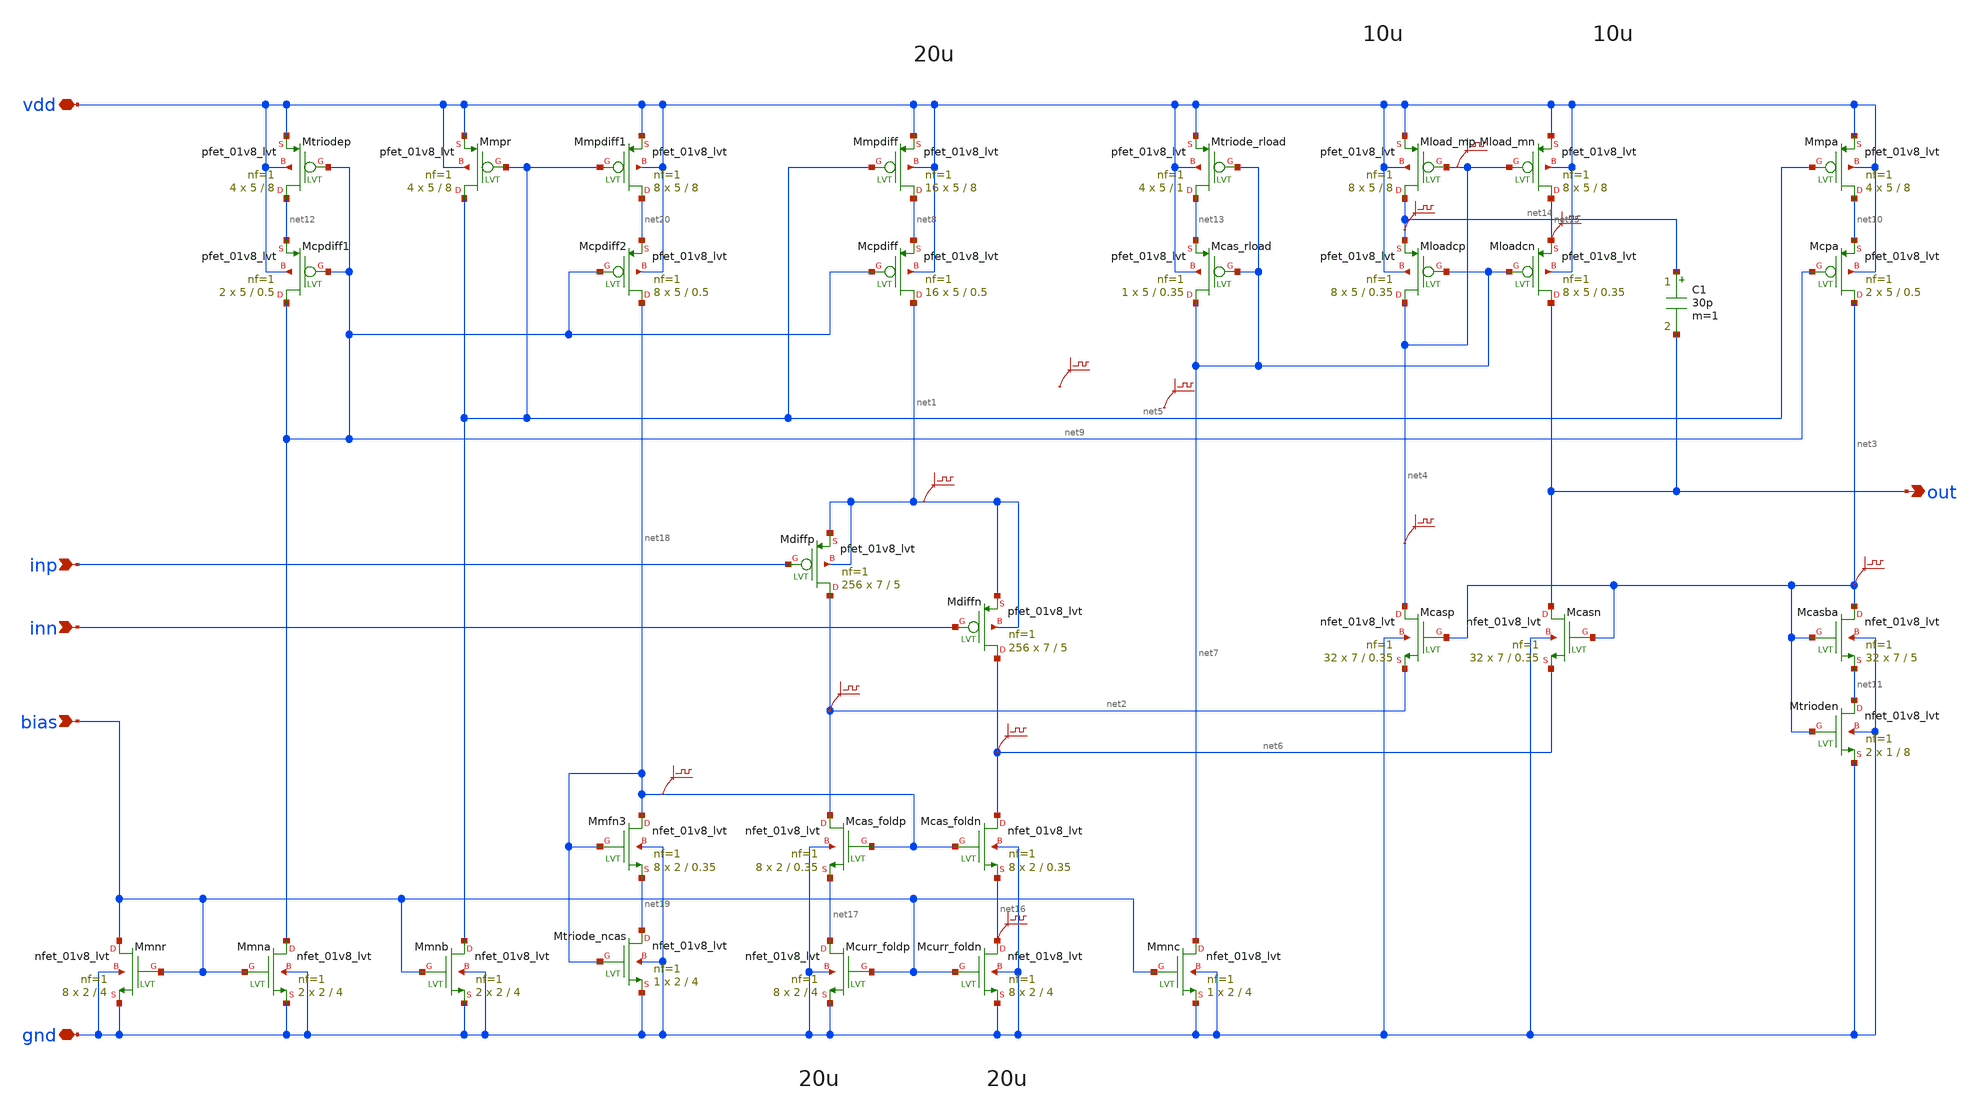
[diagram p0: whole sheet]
** sch_path: design/bandgap_opamp_twostage/bandgap_opamp_twostage.sch
**.subckt bandgap_opamp_twostage inp inn bias out vdd gnd
*.ipin inp
*.ipin inn
*.ipin bias
*.opin out
*.iopin vdd
*.iopin gnd
XMmpdiff net8 net5 vdd vdd sky130_fd_pr__pfet_01v8_lvt L=8 W=5 nf=1 ad='W * 0.29' as='W * 0.29' pd='2 * (W + 0.29)'
+ ps='2 * (W + 0.29)' nrd='0.29 / W' nrs='0.29 / W' sa=0 sb=0 sd=0 mult=16 m=16
XMmpr net5 net5 vdd vdd sky130_fd_pr__pfet_01v8_lvt L=8 W=5 nf=1 ad='W * 0.29' as='W * 0.29' pd='2 * (W + 0.29)'
+ ps='2 * (W + 0.29)' nrd='0.29 / W' nrs='0.29 / W' sa=0 sb=0 sd=0 mult=4 m=4
XMmnr bias bias gnd gnd sky130_fd_pr__nfet_01v8_lvt L=4 W=2 nf=1 ad='W * 0.29' as='W * 0.29' pd='2 * (W + 0.29)'
+ ps='2 * (W + 0.29)' nrd='0.29 / W' nrs='0.29 / W' sa=0 sb=0 sd=0 mult=8 m=8
XMmnb net5 bias gnd gnd sky130_fd_pr__nfet_01v8_lvt L=4 W=2 nf=1 ad='W * 0.29' as='W * 0.29' pd='2 * (W + 0.29)'
+ ps='2 * (W + 0.29)' nrd='0.29 / W' nrs='0.29 / W' sa=0 sb=0 sd=0 mult=2 m=2
XMtrioden net11 net3 gnd gnd sky130_fd_pr__nfet_01v8_lvt L=8 W=1 nf=1 ad='W * 0.29' as='W * 0.29' pd='2 * (W + 0.29)'
+ ps='2 * (W + 0.29)' nrd='0.29 / W' nrs='0.29 / W' sa=0 sb=0 sd=0 mult=2 m=2
XMmpa net10 net5 vdd vdd sky130_fd_pr__pfet_01v8_lvt L=8 W=5 nf=1 ad='W * 0.29' as='W * 0.29' pd='2 * (W + 0.29)'
+ ps='2 * (W + 0.29)' nrd='0.29 / W' nrs='0.29 / W' sa=0 sb=0 sd=0 mult=4 m=4
XMcpdiff net1 net9 net8 vdd sky130_fd_pr__pfet_01v8_lvt L=0.5 W=5 nf=1 ad='W * 0.29' as='W * 0.29' pd='2 * (W + 0.29)'
+ ps='2 * (W + 0.29)' nrd='0.29 / W' nrs='0.29 / W' sa=0 sb=0 sd=0 mult=16 m=16
XMmna net9 bias gnd gnd sky130_fd_pr__nfet_01v8_lvt L=4 W=2 nf=1 ad='W * 0.29' as='W * 0.29' pd='2 * (W + 0.29)'
+ ps='2 * (W + 0.29)' nrd='0.29 / W' nrs='0.29 / W' sa=0 sb=0 sd=0 mult=2 m=2
XMtriodep net12 net9 vdd vdd sky130_fd_pr__pfet_01v8_lvt L=8 W=5 nf=1 ad='W * 0.29' as='W * 0.29' pd='2 * (W + 0.29)'
+ ps='2 * (W + 0.29)' nrd='0.29 / W' nrs='0.29 / W' sa=0 sb=0 sd=0 mult=4 m=4
XMcpa net3 net9 net10 vdd sky130_fd_pr__pfet_01v8_lvt L=0.5 W=5 nf=1 ad='W * 0.29' as='W * 0.29' pd='2 * (W + 0.29)'
+ ps='2 * (W + 0.29)' nrd='0.29 / W' nrs='0.29 / W' sa=0 sb=0 sd=0 mult=2 m=2
XMcasba net3 net3 net11 gnd sky130_fd_pr__nfet_01v8_lvt L=5 W=7 nf=1 ad='W * 0.29' as='W * 0.29' pd='2 * (W + 0.29)'
+ ps='2 * (W + 0.29)' nrd='0.29 / W' nrs='0.29 / W' sa=0 sb=0 sd=0 mult=32 m=32
.save v(net2)
XMcasn out net3 net6 gnd sky130_fd_pr__nfet_01v8_lvt L=0.35 W=7 nf=1 ad='W * 0.29' as='W * 0.29' pd='2 * (W + 0.29)'
+ ps='2 * (W + 0.29)' nrd='0.29 / W' nrs='0.29 / W' sa=0 sb=0 sd=0 mult=32 m=32
XMcasp net4 net3 net2 gnd sky130_fd_pr__nfet_01v8_lvt L=0.35 W=7 nf=1 ad='W * 0.29' as='W * 0.29' pd='2 * (W + 0.29)'
+ ps='2 * (W + 0.29)' nrd='0.29 / W' nrs='0.29 / W' sa=0 sb=0 sd=0 mult=32 m=32
XMload_mp net14 net4 vdd vdd sky130_fd_pr__pfet_01v8_lvt L=8 W=5 nf=1 ad='W * 0.29' as='W * 0.29' pd='2 * (W + 0.29)'
+ ps='2 * (W + 0.29)' nrd='0.29 / W' nrs='0.29 / W' sa=0 sb=0 sd=0 mult=8 m=8
XMload_mn net15 net4 vdd vdd sky130_fd_pr__pfet_01v8_lvt L=8 W=5 nf=1 ad='W * 0.29' as='W * 0.29' pd='2 * (W + 0.29)'
+ ps='2 * (W + 0.29)' nrd='0.29 / W' nrs='0.29 / W' sa=0 sb=0 sd=0 mult=8 m=8
XMloadcn out net7 net15 vdd sky130_fd_pr__pfet_01v8_lvt L=0.35 W=5 nf=1 ad='W * 0.29' as='W * 0.29' pd='2 * (W + 0.29)'
+ ps='2 * (W + 0.29)' nrd='0.29 / W' nrs='0.29 / W' sa=0 sb=0 sd=0 mult=8 m=8
XMloadcp net4 net7 net14 vdd sky130_fd_pr__pfet_01v8_lvt L=0.35 W=5 nf=1 ad='W * 0.29' as='W * 0.29'
+ pd='2 * (W + 0.29)' ps='2 * (W + 0.29)' nrd='0.29 / W' nrs='0.29 / W' sa=0 sb=0 sd=0 mult=8 m=8
XMcurr_foldn net16 bias gnd gnd sky130_fd_pr__nfet_01v8_lvt L=4 W=2 nf=1 ad='W * 0.29' as='W * 0.29'
+ pd='2 * (W + 0.29)' ps='2 * (W + 0.29)' nrd='0.29 / W' nrs='0.29 / W' sa=0 sb=0 sd=0 mult=8 m=8
XMcurr_foldp net17 bias gnd gnd sky130_fd_pr__nfet_01v8_lvt L=4 W=2 nf=1 ad='W * 0.29' as='W * 0.29'
+ pd='2 * (W + 0.29)' ps='2 * (W + 0.29)' nrd='0.29 / W' nrs='0.29 / W' sa=0 sb=0 sd=0 mult=8 m=8
XMdiffn net6 inn net1 net1 sky130_fd_pr__pfet_01v8_lvt L=5 W=7 nf=1 ad='W * 0.29' as='W * 0.29' pd='2 * (W + 0.29)'
+ ps='2 * (W + 0.29)' nrd='0.29 / W' nrs='0.29 / W' sa=0 sb=0 sd=0 mult=256 m=256
XMdiffp net2 inp net1 net1 sky130_fd_pr__pfet_01v8_lvt L=5 W=7 nf=1 ad='W * 0.29' as='W * 0.29' pd='2 * (W + 0.29)'
+ ps='2 * (W + 0.29)' nrd='0.29 / W' nrs='0.29 / W' sa=0 sb=0 sd=0 mult=256 m=256
.save v(net3)
.save v(net1)
.save v(net21)
.save v(net22)
.save v(net15)
.save v(net4)
XMcpdiff1 net9 net9 net12 vdd sky130_fd_pr__pfet_01v8_lvt L=0.5 W=5 nf=1 ad='W * 0.29' as='W * 0.29'
+ pd='2 * (W + 0.29)' ps='2 * (W + 0.29)' nrd='0.29 / W' nrs='0.29 / W' sa=0 sb=0 sd=0 mult=2 m=2
.save v(net6)
XMtriode_rload net13 net7 vdd vdd sky130_fd_pr__pfet_01v8_lvt L=1 W=5 nf=1 ad='W * 0.29' as='W * 0.29'
+ pd='2 * (W + 0.29)' ps='2 * (W + 0.29)' nrd='0.29 / W' nrs='0.29 / W' sa=0 sb=0 sd=0 mult=4 m=4
XMcas_rload net7 net7 net13 vdd sky130_fd_pr__pfet_01v8_lvt L=0.35 W=5 nf=1 ad='W * 0.29' as='W * 0.29'
+ pd='2 * (W + 0.29)' ps='2 * (W + 0.29)' nrd='0.29 / W' nrs='0.29 / W' sa=0 sb=0 sd=0 mult=1 m=1
XMmnc net7 bias gnd gnd sky130_fd_pr__nfet_01v8_lvt L=4 W=2 nf=1 ad='W * 0.29' as='W * 0.29' pd='2 * (W + 0.29)'
+ ps='2 * (W + 0.29)' nrd='0.29 / W' nrs='0.29 / W' sa=0 sb=0 sd=0 mult=1 m=1
XMcas_foldn net6 net18 net16 gnd sky130_fd_pr__nfet_01v8_lvt L=0.35 W=2 nf=1 ad='W * 0.29' as='W * 0.29'
+ pd='2 * (W + 0.29)' ps='2 * (W + 0.29)' nrd='0.29 / W' nrs='0.29 / W' sa=0 sb=0 sd=0 mult=8 m=8
XMcas_foldp net2 net18 net17 gnd sky130_fd_pr__nfet_01v8_lvt L=0.35 W=2 nf=1 ad='W * 0.29' as='W * 0.29'
+ pd='2 * (W + 0.29)' ps='2 * (W + 0.29)' nrd='0.29 / W' nrs='0.29 / W' sa=0 sb=0 sd=0 mult=8 m=8
XMmfn3 net18 net18 net19 gnd sky130_fd_pr__nfet_01v8_lvt L=0.35 W=2 nf=1 ad='W * 0.29' as='W * 0.29'
+ pd='2 * (W + 0.29)' ps='2 * (W + 0.29)' nrd='0.29 / W' nrs='0.29 / W' sa=0 sb=0 sd=0 mult=8 m=8
XMtriode_ncas net19 net18 gnd gnd sky130_fd_pr__nfet_01v8_lvt L=4 W=2 nf=1 ad='W * 0.29' as='W * 0.29'
+ pd='2 * (W + 0.29)' ps='2 * (W + 0.29)' nrd='0.29 / W' nrs='0.29 / W' sa=0 sb=0 sd=0 mult=1 m=1
XMmpdiff1 net20 net5 vdd vdd sky130_fd_pr__pfet_01v8_lvt L=8 W=5 nf=1 ad='W * 0.29' as='W * 0.29' pd='2 * (W + 0.29)'
+ ps='2 * (W + 0.29)' nrd='0.29 / W' nrs='0.29 / W' sa=0 sb=0 sd=0 mult=8 m=8
XMcpdiff2 net18 net9 net20 vdd sky130_fd_pr__pfet_01v8_lvt L=0.5 W=5 nf=1 ad='W * 0.29' as='W * 0.29'
+ pd='2 * (W + 0.29)' ps='2 * (W + 0.29)' nrd='0.29 / W' nrs='0.29 / W' sa=0 sb=0 sd=0 mult=8 m=8
.save v(net18)
.save v(net16)
.save v(net4)
C1 net14 out 30p m=1
.save v(net14)
**.ends
.end
